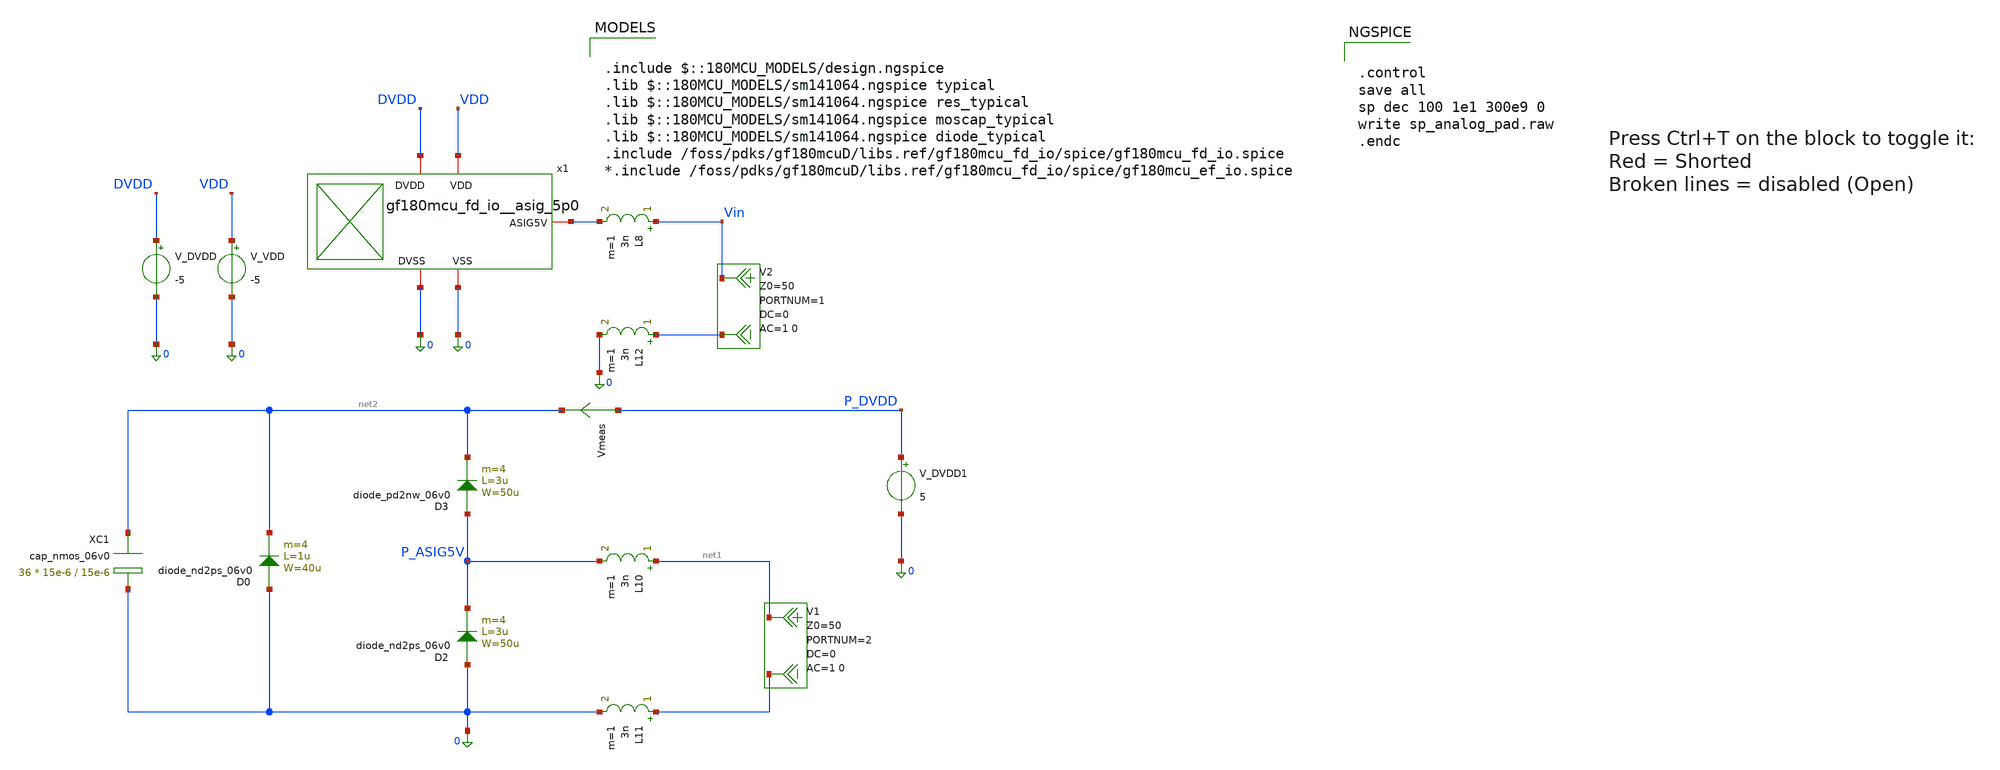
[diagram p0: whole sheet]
** sch_path: Pads_Simulation/schematic_sp.sch
**.subckt schematic_sp
x1 DVDD Vin 0 VDD 0 gf180mcu_fd_io__asig_5p0
V_VDD VDD 0 -5
V_DVDD DVDD 0 -5
V1 net1 0 DC 0 AC 1 0 portnum 2 z0 50
V2 Vin 0 DC 0 AC 1 0 portnum 1 z0 50
D0 0 net2 diode_nd2ps_06v0 area='40u * 1u ' pj='2*40u + 2*1u ' m=4
D2 0 P_ASIG5V diode_nd2ps_06v0 area='50u * 3u ' pj='2*50u + 2*3u ' m=4
D3 P_ASIG5V net2 diode_pd2nw_06v0 area='50u * 3u ' pj='2*50u + 2*3u ' m=4
XC1 net2 0 cap_nmos_06v0 c_width=15e-6 c_length=15e-6 m=36
Vmeas P_DVDD net2 0
.save i(vmeas)
V_DVDD1 P_DVDD 0 5
L10 net1 P_ASIG5V 3n m=1
**** begin user architecture code


.control
save all
sp dec 100 1e1 300e9 0
write sp_analog_pad.raw
.endc



.include $::180MCU_MODELS/design.ngspice
.lib $::180MCU_MODELS/sm141064.ngspice typical
.lib $::180MCU_MODELS/sm141064.ngspice res_typical
.lib $::180MCU_MODELS/sm141064.ngspice moscap_typical
.lib $::180MCU_MODELS/sm141064.ngspice diode_typical
.include /foss/pdks/gf180mcuD/libs.ref/gf180mcu_fd_io/spice/gf180mcu_fd_io.spice
*.include /foss/pdks/gf180mcuD/libs.ref/gf180mcu_fd_io/spice/gf180mcu_ef_io.spice

**** end user architecture code
**.ends
.end
